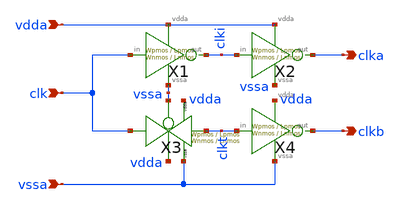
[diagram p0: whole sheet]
** sch_path: xschem/clkgen/comp_clks.sch
**.subckt comp_clks clk clka clkb vdda vssa
*.ipin clk
*.opin clka
*.opin clkb
*.ipin vdda
*.ipin vssa
X3 clk clkt vssa vdda vdda vssa transmission_gate Wpmos=Wpmos Lpmos=Lpmos Wnmos=Wnmos Lnmos=Lnmos
X1 clk clki vdda vssa inv Wpmos=Wpmos Lpmos=Lpmos Wnmos=Wnmos Lnmos=Lnmos
X2 clki clka vdda vssa inv Wpmos=Wpmos Lpmos=Lpmos Wnmos=Wnmos Lnmos=Lnmos
X4 clkt clkb vdda vssa inv Wpmos=Wpmos Lpmos=Lpmos Wnmos=Wnmos Lnmos=Lnmos
**.ends

* expanding   symbol:  transmission_gate/transmission_gate.sym # of pins=6
** sym_path: xschem/transmission_gate/transmission_gate.sym
** sch_path: xschem/transmission_gate/transmission_gate.sch
.subckt transmission_gate in out ctrl_ ctrl vdda vssa  Wpmos=Wpmos Lpmos=Lpmos Wnmos=Wnmos
+ Lnmos=Lnmos
*.iopin in
*.iopin out
*.ipin ctrl_
*.ipin ctrl
*.ipin vdda
*.ipin vssa
XM1 out ctrl in vssa sky130_fd_pr__nfet_01v8 L=Lnmos W=Wnmos nf=1 ad='int((nf+1)/2) * W/nf * 0.29' as='int((nf+2)/2) * W/nf * 0.29'
+ pd='2*int((nf+1)/2) * (W/nf + 0.29)' ps='2*int((nf+2)/2) * (W/nf + 0.29)' nrd='0.29 / W' nrs='0.29 / W'
+ sa=0 sb=0 sd=0 mult=1 m=1
XM2 out ctrl_ in vdda sky130_fd_pr__pfet_01v8 L=Lpmos W=Wpmos nf=1 ad='int((nf+1)/2) * W/nf * 0.29' as='int((nf+2)/2) * W/nf * 0.29'
+ pd='2*int((nf+1)/2) * (W/nf + 0.29)' ps='2*int((nf+2)/2) * (W/nf + 0.29)' nrd='0.29 / W' nrs='0.29 / W'
+ sa=0 sb=0 sd=0 mult=1 m=1
.ends


* expanding   symbol:  xschem/inv/inv.sym # of pins=4
** sym_path: xschem/inv/inv.sym
** sch_path: xschem/inv/inv.sch
.subckt inv in out vdda vssa  Wpmos=Wpmos Lpmos=Lpmos Wnmos=Wnmos Lnmos=Lnmos
*.ipin in
*.iopin out
*.ipin vdda
*.ipin vssa
XM1 vssa in out vssa sky130_fd_pr__nfet_01v8 L=Lnmos W=Wnmos nf=1 ad='int((nf+1)/2) * W/nf * 0.29' as='int((nf+2)/2) * W/nf * 0.29'
+ pd='2*int((nf+1)/2) * (W/nf + 0.29)' ps='2*int((nf+2)/2) * (W/nf + 0.29)' nrd='0.29 / W' nrs='0.29 / W'
+ sa=0 sb=0 sd=0 mult=1 m=1
XM2 vdda in out vdda sky130_fd_pr__pfet_01v8 L=Lpmos W=Wpmos nf=1 ad='int((nf+1)/2) * W/nf * 0.29' as='int((nf+2)/2) * W/nf * 0.29'
+ pd='2*int((nf+1)/2) * (W/nf + 0.29)' ps='2*int((nf+2)/2) * (W/nf + 0.29)' nrd='0.29 / W' nrs='0.29 / W'
+ sa=0 sb=0 sd=0 mult=1 m=1
.ends

.end
